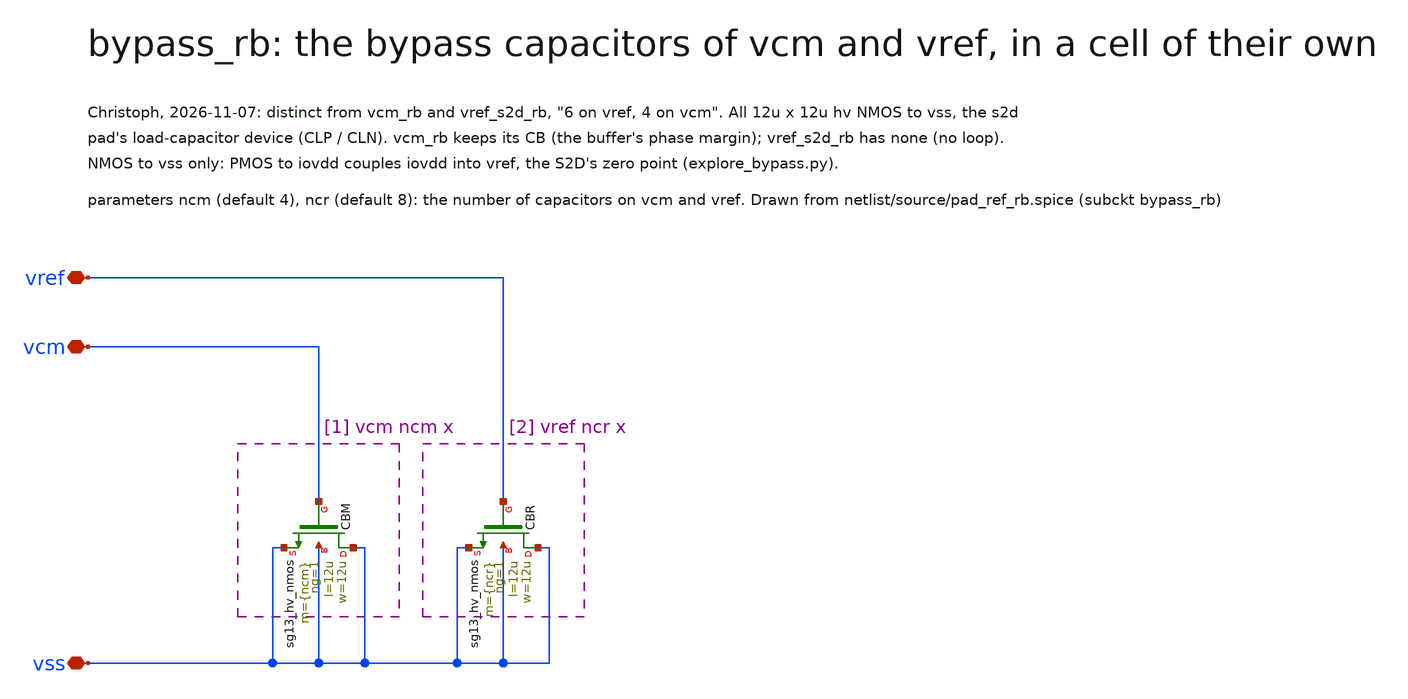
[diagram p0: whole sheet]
** sch_path: macros/pad_ref_rb/schematic/xschem/bypass_rb.sch
**.subckt bypass_rb vss vcm vref
*.iopin vss
*.iopin vcm
*.iopin vref
XCBM vss vcm vss vss sg13_hv_nmos w=12u l=12u ng=1 m={ncm} mm_ok=1
XCBR vss vref vss vss sg13_hv_nmos w=12u l=12u ng=1 m={ncr} mm_ok=1
**.ends
.end
